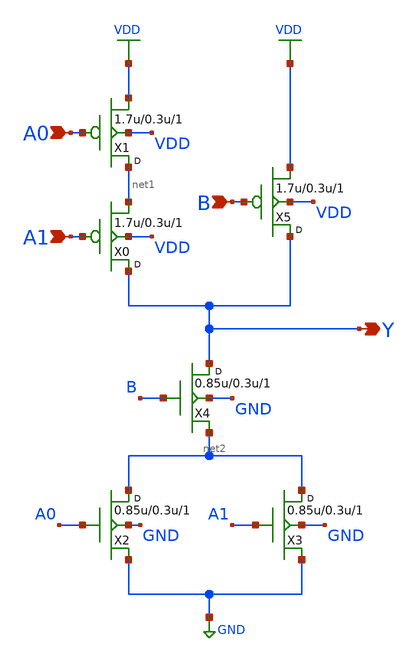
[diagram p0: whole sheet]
** sch_path: openfasoc/common/platforms/gf180mcuosu9Toai211/gf180mcu_osu_sc_oai21_1.sch
**.subckt gf180mcu_osu_sc_oai21_1 A0 A1 Y B
*.ipin A0
*.ipin A1
*.opin Y
*.ipin B
X1 net1 A0 VDD VDD pmos_3p3 w=1.7u l=0.3u m=1
X0 Y A1 net1 VDD pmos_3p3 w=1.7u l=0.3u m=1
X2 net2 A0 GND GND nmos_3p3 w=0.85u l=0.3u m=1
X3 net2 A1 GND GND nmos_3p3 w=0.85u l=0.3u m=1
X4 Y B net2 GND nmos_3p3 w=0.85u l=0.3u m=1
X5 Y B VDD VDD pmos_3p3 w=1.7u l=0.3u m=1
**.ends
.GLOBAL VDD
.GLOBAL GND
.end
